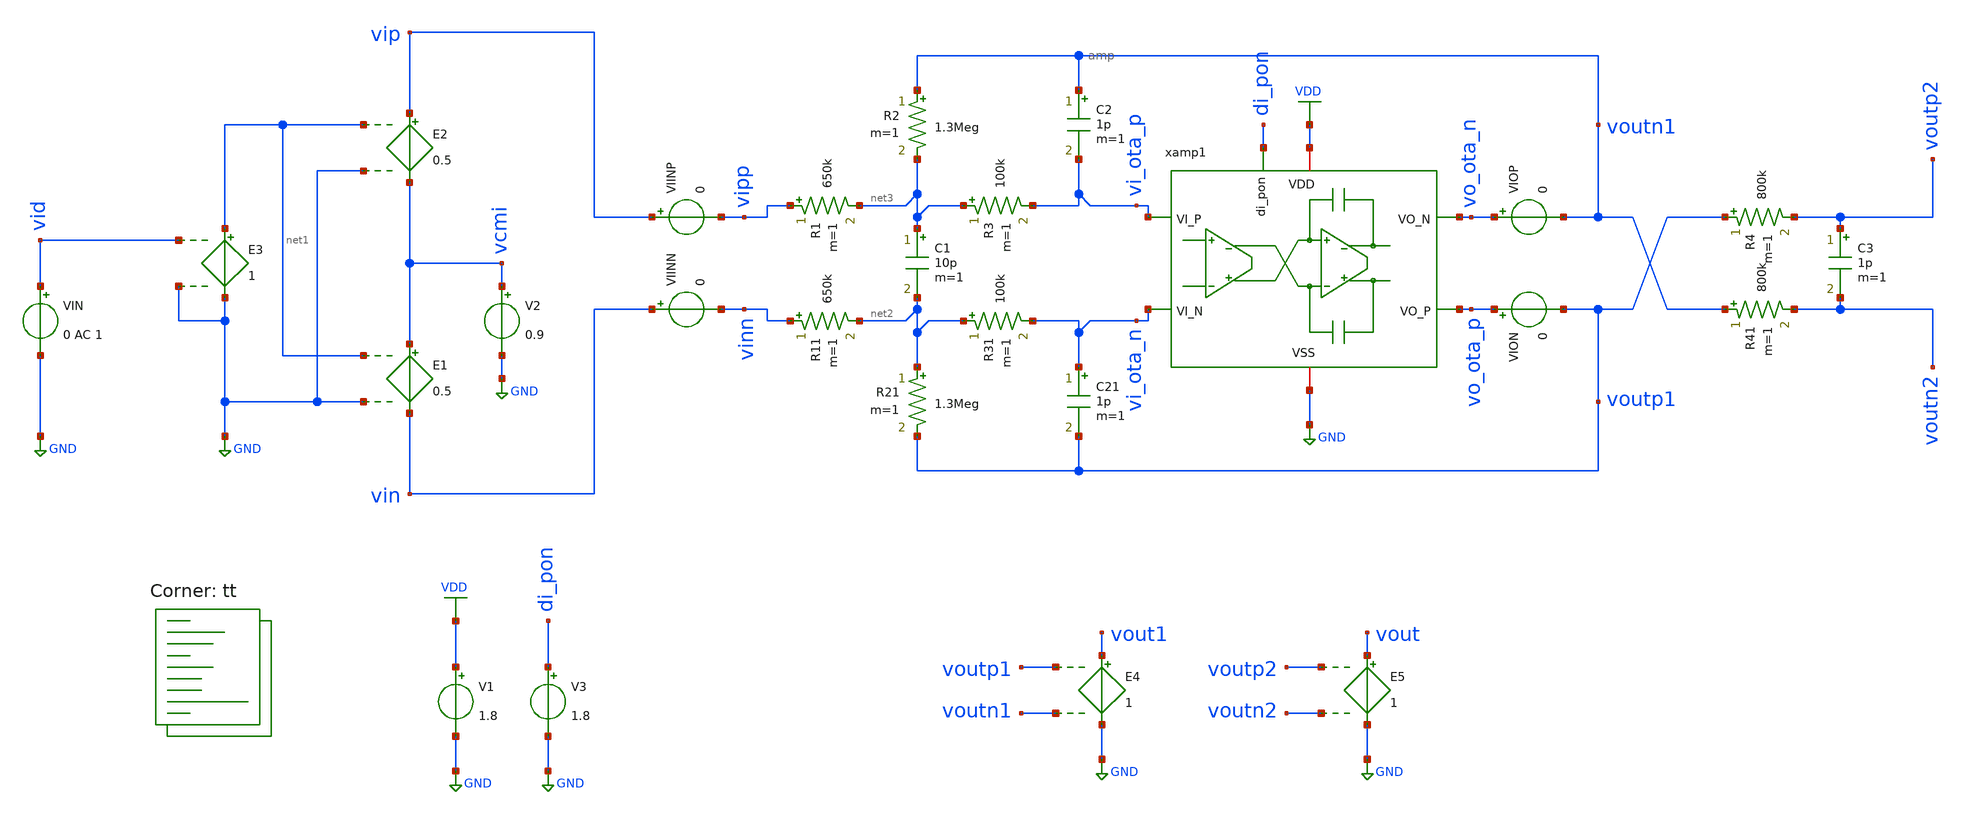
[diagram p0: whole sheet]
** sch_path: xschem/tb_filter_cl.sch
**.subckt tb_filter_cl
V2 vcmi GND 0.9
E1 vcmi vin net1 GND 0.5
E2 vip vcmi net1 GND 0.5
VIN vid GND 0 AC 1
E3 net1 GND vid GND 1
E4 vout1 GND voutp1 voutn1 1
VIINP vip vipp 0
VIINN vin vinn 0
R1 vipp net3 650k m=1
R2 voutn1 net3 1.3Meg m=1
R3 net3 vi_ota_p 100k m=1
C1 net3 net2 10p m=1
C3 voutp2 voutn2 1p m=1
R11 vinn net2 650k m=1
R21 net2 voutp1 1.3Meg m=1
R31 net2 vi_ota_n 100k m=1
C21 vi_ota_n voutp1 1p m=1
R4 voutp1 voutp2 800k m=1
R41 voutn1 voutn2 800k m=1
C2 voutn1 vi_ota_p 1p m=1
E5 vout GND voutp2 voutn2 1
VIOP vo_ota_n voutn1 0
VION vo_ota_p voutp1 0
xamp1 VDD vi_ota_n vi_ota_p vo_ota_p di_pon vo_ota_n GND amp
V1 VDD GND 1.8
V3 di_pon GND 1.8
**** begin user architecture code
.lib $::SKYWATER_MODELS/sky130.lib.spice tt


*.include /foss/designs/filter/amp_dev_save.spice
.options savecurrents
.options method=gear reltol=.005
.options sparse
.control
save all

let f_min = 10
let f_max = 100Meg
let f_stop = 500k

let Adc = 2
let err_gain_spec = 0.004
let v_step_o = 0.9
let v_step_i = v_step_o/Adc

let t_rf = 0.1u
let t_step = 50u
let t_delay = 0
let t_per = 2*t_step

let tstep = 0.1*t_rf
let tstop = 2*t_per
let tstart = t_delay

*alter @VIN[SIN] = [ 0 0.01 $&f_sig 0 0 0 ]
alter @VIN[DC] = 0.0


*set fndc = /foss/designs/frontend/frontend_dc.txt
*set fntran = /foss/designs/frontend/frontend_tran.txt
*set fnspec = /foss/designs/frontend/frontend_spec.txt
*set fnhd = /foss/designs/frontend/frontend_hd.txt
*set fnnoise = /foss/designs/frontend/frontend_noise.txt
set wr_singlescale
set wr_vecnames
option numdgt=3

set opSimOnly = 0


** Main Simulations
if $opSimOnly eq 0
	op
	ac dec 100 $&const.f_min $&const.f_max
	*set sqrnoise
	noise v(vout) VIN dec 100 $&const.f_min $&const.f_max 1
	noise v(vout) VIN dec 10 1 50Meg
	alter @VIN[PULSE] = [ 0 $&v_step_i $&t_delay $&t_rf $&t_rf $&t_step $&t_per 0 ]
	** Check power on by ramping Vdd, tie di_pon to VDD net!
	*alter @V1[PULSE] = [ 0 1.8 0 10u $&t_rf 0 0 0 ]
	tran $&tstep $&tstop $&tstart

	setplot ac1
	let A1 = v(vout1)/v(vid)
	let A2 = v(vout)/v(vid)

	let Amag_dB = vdb(A2)
	settype decibel Amag_dB
	let Aarg = 180/PI*cphase(A2)

	let fdc = const.f_min+1
	meas ac Adc_ol_dB find Amag_dB when frequency = fdc
	let Amag_fc = Adc_ol_dB-3
	meas ac fc find frequency when Amag_dB = Amag_fc
	meas ac Amin min_at Amag_dB from=const.f_min to=fc
	meas ac Amax max Amag_dB
	meas ac Astop find Amag_dB when frequency = const.f_stop

	meas ac fug find frequency when Amag_dB=0
	let err_gain_act = 1-10^(Adc_ol_dB/20)/Adc
	let Adc_ol_min = Adc*(1-err_gain_spec)/err_gain_spec
	let Adc_ol_min_dB = vdb(Adc_ol_min)
	print err_gain_act*100
	print Adc_ol_min_dB
	plot Amag_dB Aarg ylabel 'Magnitude, Phase'

	setplot noise1
	let acgain = onoise_spectrum/inoise_spectrum
	let r1 = sqrt(2)*onoise_r1
	let r2 = sqrt(2)*onoise_r2
	let r3 = sqrt(2)*onoise_r3
	let r4 = sqrt(2)*onoise_r4
	let diffpair = sqrt(2)*onoise.m.xamp1.xmp4.msky130_fd_pr__pfet_01v8
	let load_n = sqrt(2)*onoise.m.xamp1.xmn1.msky130_fd_pr__nfet_01v8
	let load_p = sqrt(2)*onoise.m.xamp1.xmp7.msky130_fd_pr__pfet_01v8
	let comsource = sqrt(2)*onoise.m.xamp1.xmn3.msky130_fd_pr__nfet_01v8
	*plot inoise_spectrum ylog xlog
	plot onoise_spectrum r1 r2 r3 r4 diffpair load_n load_p comsource ylog xlog ylabel 'Output Noise'

	setplot noise4
	let p_noise_q = (1e-3)^2
	let p_noise_o = onoise_total^2
	let p_sig_o = (v_step_o/(2*sqrt(2)))^2
	let snr = p_sig_o/(p_noise_o+p_noise_q)
	let snr_dB = 10*log10(snr)
	print snr_dB

	setplot tran4
	let vid = v(vid)
	let iop = viop#branch
	let ion = vion#branch
	let vcmo = (voutp1+voutn1)/2

	*plot iop ion

	plot vid vout1 vout vcmo
	plot v(vip) v(vin) v(voutp1) v(voutn1) vcmo
end

alter @VIN[DC] = 0
op

remzerovec
write tb_filter_cl.raw
.endc

**** end user architecture code
**.ends
.GLOBAL GND
.GLOBAL VDD
.end
